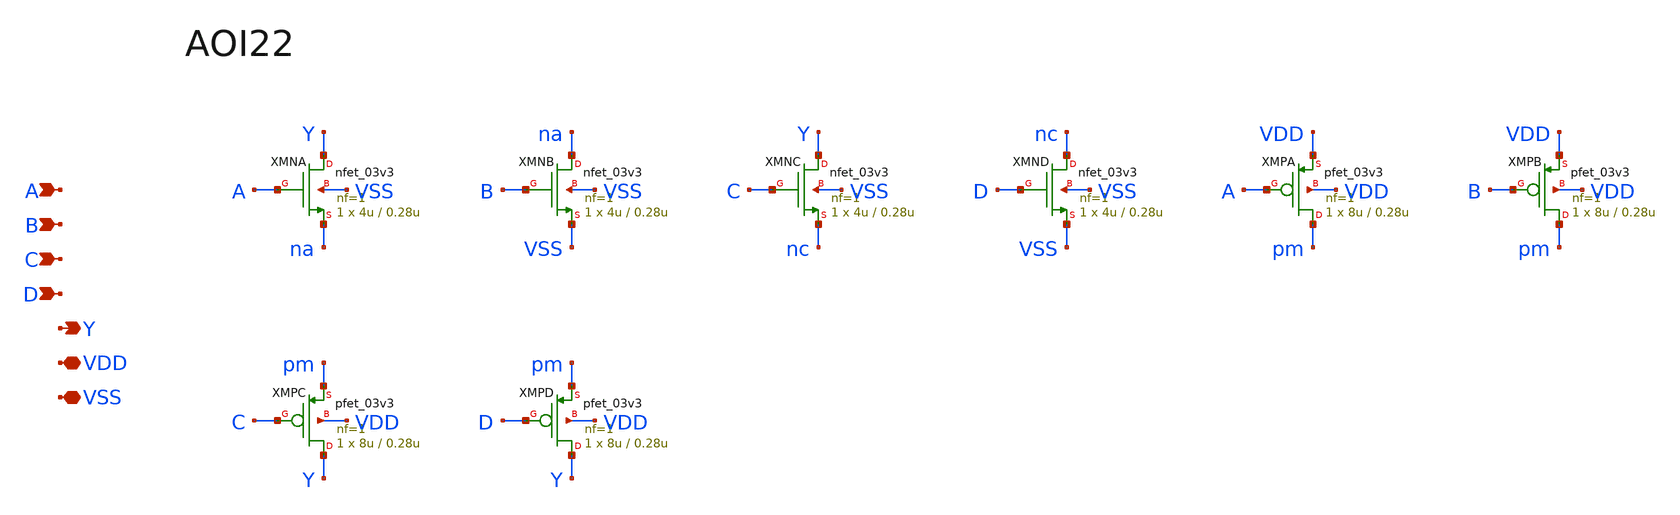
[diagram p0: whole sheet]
** sch_path: v1_claude/archive/legacy_cells/xschem/aoi22.sch
**.subckt aoi22 A B C D Y VDD VSS
*.ipin A
*.ipin B
*.ipin C
*.ipin D
*.opin Y
*.iopin VDD
*.iopin VSS
XMNA Y A na VSS nfet_03v3 L=0.28u W=4u nf=1 ad='int((nf+1)/2) * W/nf * 0.18u' as='int((nf+2)/2) * W/nf * 0.18u'
+ pd='2*int((nf+1)/2) * (W/nf + 0.18u)' ps='2*int((nf+2)/2) * (W/nf + 0.18u)' nrd='0.18u / W' nrs='0.18u / W'
+ sa=0 sb=0 sd=0 m=1
XMNB na B VSS VSS nfet_03v3 L=0.28u W=4u nf=1 ad='int((nf+1)/2) * W/nf * 0.18u' as='int((nf+2)/2) * W/nf * 0.18u'
+ pd='2*int((nf+1)/2) * (W/nf + 0.18u)' ps='2*int((nf+2)/2) * (W/nf + 0.18u)' nrd='0.18u / W' nrs='0.18u / W'
+ sa=0 sb=0 sd=0 m=1
XMNC Y C nc VSS nfet_03v3 L=0.28u W=4u nf=1 ad='int((nf+1)/2) * W/nf * 0.18u' as='int((nf+2)/2) * W/nf * 0.18u'
+ pd='2*int((nf+1)/2) * (W/nf + 0.18u)' ps='2*int((nf+2)/2) * (W/nf + 0.18u)' nrd='0.18u / W' nrs='0.18u / W'
+ sa=0 sb=0 sd=0 m=1
XMND nc D VSS VSS nfet_03v3 L=0.28u W=4u nf=1 ad='int((nf+1)/2) * W/nf * 0.18u' as='int((nf+2)/2) * W/nf * 0.18u'
+ pd='2*int((nf+1)/2) * (W/nf + 0.18u)' ps='2*int((nf+2)/2) * (W/nf + 0.18u)' nrd='0.18u / W' nrs='0.18u / W'
+ sa=0 sb=0 sd=0 m=1
XMPA pm A VDD VDD pfet_03v3 L=0.28u W=8u nf=1 ad='int((nf+1)/2) * W/nf * 0.18u' as='int((nf+2)/2) * W/nf * 0.18u'
+ pd='2*int((nf+1)/2) * (W/nf + 0.18u)' ps='2*int((nf+2)/2) * (W/nf + 0.18u)' nrd='0.18u / W' nrs='0.18u / W'
+ sa=0 sb=0 sd=0 m=1
XMPB pm B VDD VDD pfet_03v3 L=0.28u W=8u nf=1 ad='int((nf+1)/2) * W/nf * 0.18u' as='int((nf+2)/2) * W/nf * 0.18u'
+ pd='2*int((nf+1)/2) * (W/nf + 0.18u)' ps='2*int((nf+2)/2) * (W/nf + 0.18u)' nrd='0.18u / W' nrs='0.18u / W'
+ sa=0 sb=0 sd=0 m=1
XMPC Y C pm VDD pfet_03v3 L=0.28u W=8u nf=1 ad='int((nf+1)/2) * W/nf * 0.18u' as='int((nf+2)/2) * W/nf * 0.18u'
+ pd='2*int((nf+1)/2) * (W/nf + 0.18u)' ps='2*int((nf+2)/2) * (W/nf + 0.18u)' nrd='0.18u / W' nrs='0.18u / W'
+ sa=0 sb=0 sd=0 m=1
XMPD Y D pm VDD pfet_03v3 L=0.28u W=8u nf=1 ad='int((nf+1)/2) * W/nf * 0.18u' as='int((nf+2)/2) * W/nf * 0.18u'
+ pd='2*int((nf+1)/2) * (W/nf + 0.18u)' ps='2*int((nf+2)/2) * (W/nf + 0.18u)' nrd='0.18u / W' nrs='0.18u / W'
+ sa=0 sb=0 sd=0 m=1
**.ends
.end
